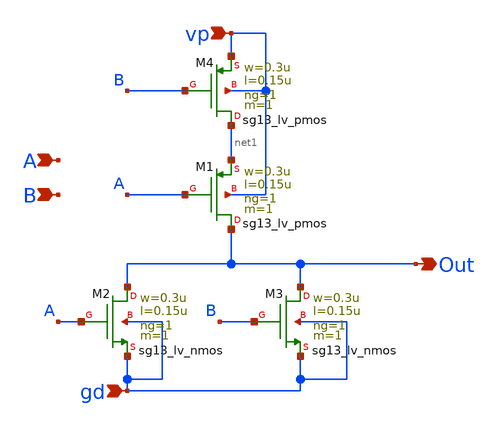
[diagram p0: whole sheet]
** sch_path: schematics/PFD/PFD_NOR.sch
**.subckt PFD_NOR vp gd B A Out
*.ipin vp
*.ipin gd
*.ipin B
*.ipin A
*.opin Out
XM1 Out A net1 vp sg13_lv_pmos w=0.3u l=0.15u ng=1 m=1 mm_ok=1
XM4 net1 B vp vp sg13_lv_pmos w=0.3u l=0.15u ng=1 m=1 mm_ok=1
XM2 Out A gd gd sg13_lv_nmos w=0.3u l=0.15u ng=1 m=1 mm_ok=1
XM3 Out B gd gd sg13_lv_nmos w=0.3u l=0.15u ng=1 m=1 mm_ok=1
**.ends
.end
